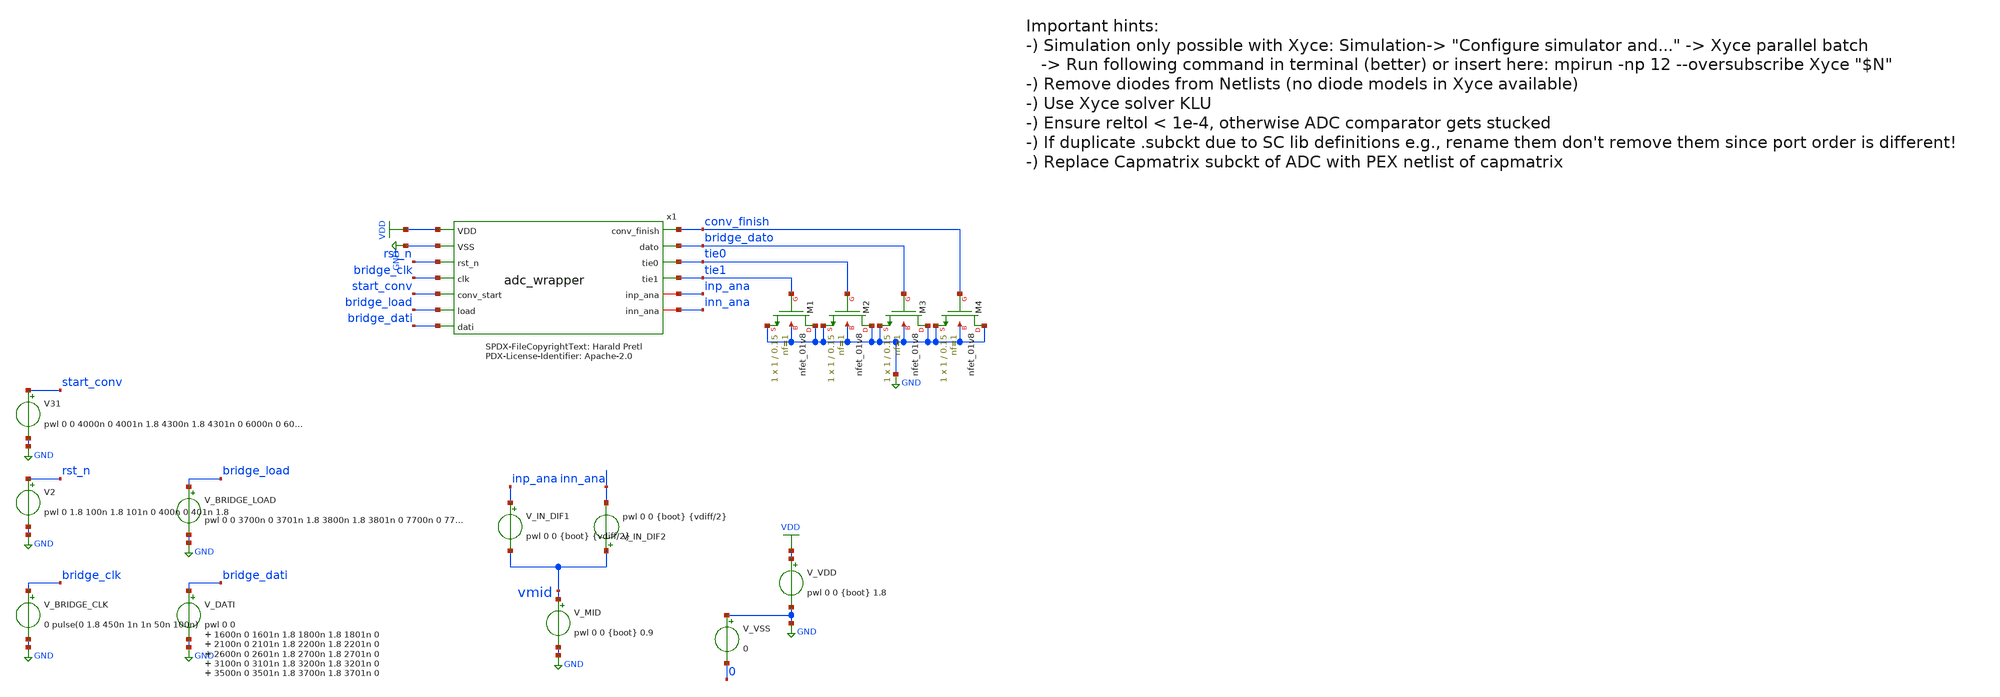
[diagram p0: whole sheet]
** sch_path: xschem/adc_wrapper_tb.sch
**.subckt adc_wrapper_tb
x1 VDD GND rst_n bridge_clk start_conv conv_finish bridge_load bridge_dati bridge_dato tie0 tie1
+ inp_ana inn_ana adc_wrapper
V_VDD VDD GND pwl 0 0 {boot} 1.8
V_VSS GND 0 0
V_MID vmid GND pwl 0 0 {boot} 0.9
V_IN_DIF1 inp_ana vmid pwl 0 0 {boot} {vdiff/2}
V_IN_DIF2 vmid inn_ana pwl 0 0 {boot} {vdiff/2}
V31 start_conv GND pwl 0 0 4000n 0 4001n 1.8 4300n 1.8 4301n 0 6000n 0 6001n 1.8 6300n 1.8 6301n 0
+ 8000n 0 8001n 1.8 8300n 1.8 8301n 0
V_DATI bridge_dati GND pwl 0 0 1600n 0 1601n 1.8 1800n 1.8 1801n 0 2100n 0 2101n 1.8 2200n 1.8 2201n
+ 0 2600n 0 2601n 1.8 2700n 1.8 2701n 0 3100n 0 3101n 1.8 3200n 1.8 3201n 0 3500n 0 3501n 1.8 3700n 1.8
+ 3701n 0
V_BRIDGE_LOAD bridge_load GND pwl 0 0 3700n 0 3701n 1.8 3800n 1.8 3801n 0 7700n 0 7701n 1.8 7800n
+ 1.8 7801n 0 10000n 0 10001n 1.8 10100n 1.8 10101n 0
V_BRIDGE_CLK bridge_clk GND 0 pulse(0 1.8 450n 1n 1n 50n 100n)
V2 rst_n GND pwl 0 1.8 100n 1.8 101n 0 400n 0 401n 1.8
XM1 GND tie1 GND GND sky130_fd_pr__nfet_01v8 L=0.15 W=1 nf=1 ad='int((nf+1)/2) * W/nf * 0.29' as='int((nf+2)/2) * W/nf * 0.29'
+ pd='2*int((nf+1)/2) * (W/nf + 0.29)' ps='2*int((nf+2)/2) * (W/nf + 0.29)' nrd='0.29 / W' nrs='0.29 / W'
+ sa=0 sb=0 sd=0 mult=1 m=1
XM2 GND tie0 GND GND sky130_fd_pr__nfet_01v8 L=0.15 W=1 nf=1 ad='int((nf+1)/2) * W/nf * 0.29' as='int((nf+2)/2) * W/nf * 0.29'
+ pd='2*int((nf+1)/2) * (W/nf + 0.29)' ps='2*int((nf+2)/2) * (W/nf + 0.29)' nrd='0.29 / W' nrs='0.29 / W'
+ sa=0 sb=0 sd=0 mult=1 m=1
XM3 GND bridge_dato GND GND sky130_fd_pr__nfet_01v8 L=0.15 W=1 nf=1 ad='int((nf+1)/2) * W/nf * 0.29'
+ as='int((nf+2)/2) * W/nf * 0.29' pd='2*int((nf+1)/2) * (W/nf + 0.29)' ps='2*int((nf+2)/2) * (W/nf + 0.29)'
+ nrd='0.29 / W' nrs='0.29 / W' sa=0 sb=0 sd=0 mult=1 m=1
XM4 GND conv_finish GND GND sky130_fd_pr__nfet_01v8 L=0.15 W=1 nf=1 ad='int((nf+1)/2) * W/nf * 0.29'
+ as='int((nf+2)/2) * W/nf * 0.29' pd='2*int((nf+1)/2) * (W/nf + 0.29)' ps='2*int((nf+2)/2) * (W/nf + 0.29)'
+ nrd='0.29 / W' nrs='0.29 / W' sa=0 sb=0 sd=0 mult=1 m=1
**** begin user architecture code

** opencircuitdesign pdks install
.lib $::SKYWATER_MODELS/sky130.lib.spice tt





**** end user architecture code
**.ends
.GLOBAL VDD
.GLOBAL GND
.end
